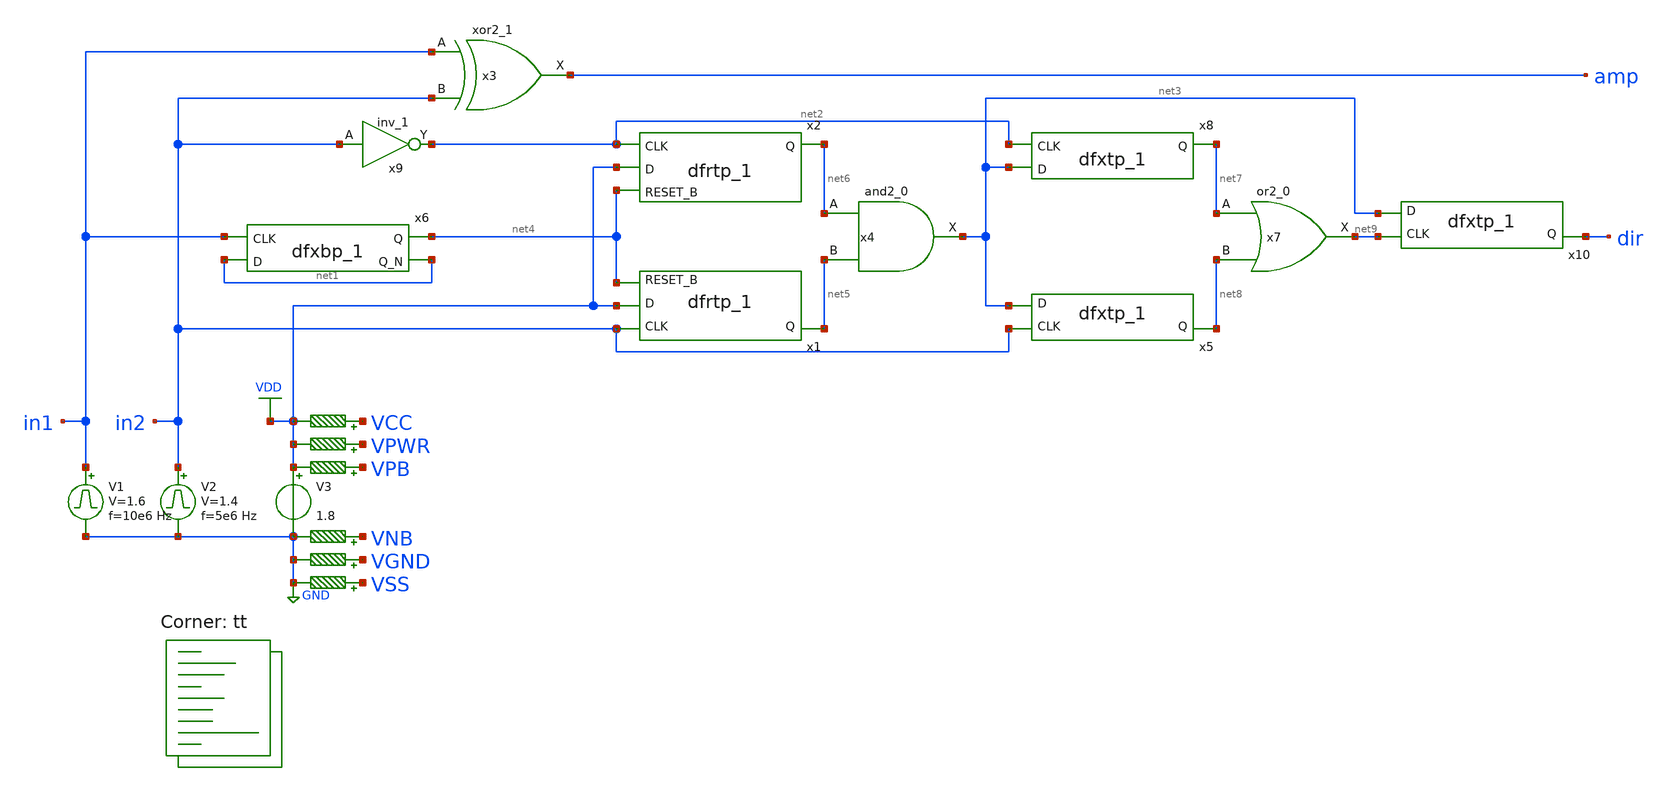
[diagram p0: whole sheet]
** sch_path: archive/PFD.sch
**.subckt PFD
V3 VDD GND 1.8
R1 VNB GND 0.01 m=1
R2 VPB VDD 0.01 m=1
R3 VPWR VDD 0.01 m=1
R4 VGND GND 0.01 m=1
V1 in1 GND pulse 0 1.6 '0.495/ 10e6 ' '0.01/10e6 ' '0.01/10e6 ' '0.49/10e6 ' '1/10e6 '
V2 in2 GND pulse 0 1.4 '0.495/ 5e6 ' '0.01/5e6 ' '0.01/5e6 ' '0.49/5e6 ' '1/5e6 '
R5 VSS GND 0.01 m=1
R6 VCC VDD 0.01 m=1
x1 in2 VDD net4 VGND VNB VPB VPWR net5 sky130_fd_sc_hd__dfrtp_1
x4 net6 net5 VGND VNB VPB VPWR net3 sky130_fd_sc_hd__and2_0
x3 in1 in2 VGND VNB VPB VPWR amp sky130_fd_sc_hd__xor2_1
x6 in1 net1 VGND VNB VPB VPWR net4 net1 sky130_fd_sc_hd__dfxbp_1
x7 net7 net8 VGND VNB VPB VPWR net9 sky130_fd_sc_hd__or2_0
x10 net9 net3 VGND VNB VPB VPWR dir sky130_fd_sc_hd__dfxtp_1
x5 in2 net3 VGND VNB VPB VPWR net8 sky130_fd_sc_hd__dfxtp_1
x8 net2 net3 VGND VNB VPB VPWR net7 sky130_fd_sc_hd__dfxtp_1
x9 in2 VGND VNB VPB VPWR net2 sky130_fd_sc_hd__inv_1
x2 net2 VDD net4 VGND VNB VPB VPWR net6 sky130_fd_sc_hd__dfrtp_1
**** begin user architecture code
.lib $::SKYWATER_MODELS/sky130.lib.spice tt


.include /usr/local/share/pdk/sky130A/libs.ref/sky130_fd_sc_hd/spice/sky130_fd_sc_hd.spice tt
.control
  save all
  tran 1n 1u
  write top.raw
  quit 0
.endc


**** end user architecture code
**.ends
.GLOBAL GND
.GLOBAL VDD
.end
